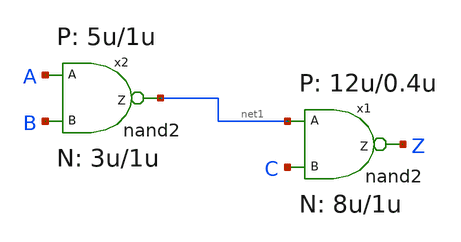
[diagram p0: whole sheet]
** sch_path: xschem-src/xschem_library/examples/test2.sch
* Copyright (C) 1998-2026 Stefan Frederik Schippers
* This program is free software; you can redistribute it and/or modify
* it under the terms of the GNU General Public License as published by
* the Free Software Foundation; either version 2 of the License, or
* (at your option) any later version.
* This program is distributed in the hope that it will be useful,
* but WITHOUT ANY WARRANTY; without even the implied warranty of
* MERCHANTABILITY or FITNESS FOR A PARTICULAR PURPOSE.  See the
* GNU General Public License for more details.
* You should have received a copy of the GNU General Public License
* along with this program; if not, write to the Free Software
**.subckt test2
x1 Z net1 C nand2 WP=12u LP=0.4u WN=8u LLN=1u
x2 net1 A B nand2 WP=5u LP=1u WN=3u LLN=1u
**.ends

* expanding   symbol:  nand2.sym # of pins=3
** sym_path: xschem-src/xschem_library/examples/nand2.sym
** sch_path: xschem-src/xschem_library/examples/nand2.sch
.subckt nand2 Z A B  WP=8u LP=1u WN=5u LLN=1u
*.ipin A
*.opin Z
*.ipin B
m1 Z A net1 VSS CMOSN w=WN l=LLN m=1
m1 net1 B VSS VSS CMOSN w=WN l=LLN m=1
m2 Z B VCC VCC CMOSP w=WP l=LP m=1
m2 Z A VCC VCC CMOSP w=WP l=LP m=1
.ends

.GLOBAL VSS
.GLOBAL VCC
.end
